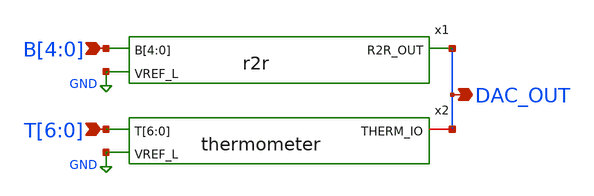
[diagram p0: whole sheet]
** sch_path: xschem/8_bit_dac.sch
**.subckt 8_bit_dac DAC_OUT B[4],B[3],B[2],B[1],B[0] T[6],T[5],T[4],T[3],T[2],T[1],T[0]
*.opin DAC_OUT
*.ipin B[4],B[3],B[2],B[1],B[0]
*.ipin T[6],T[5],T[4],T[3],T[2],T[1],T[0]
x1 B[4] B[3] B[2] B[1] B[0] GND DAC_OUT r2r
x2 DAC_OUT GND T[6] T[5] T[4] T[3] T[2] T[1] T[0] thermometer
**.ends
.GLOBAL GND
.end
